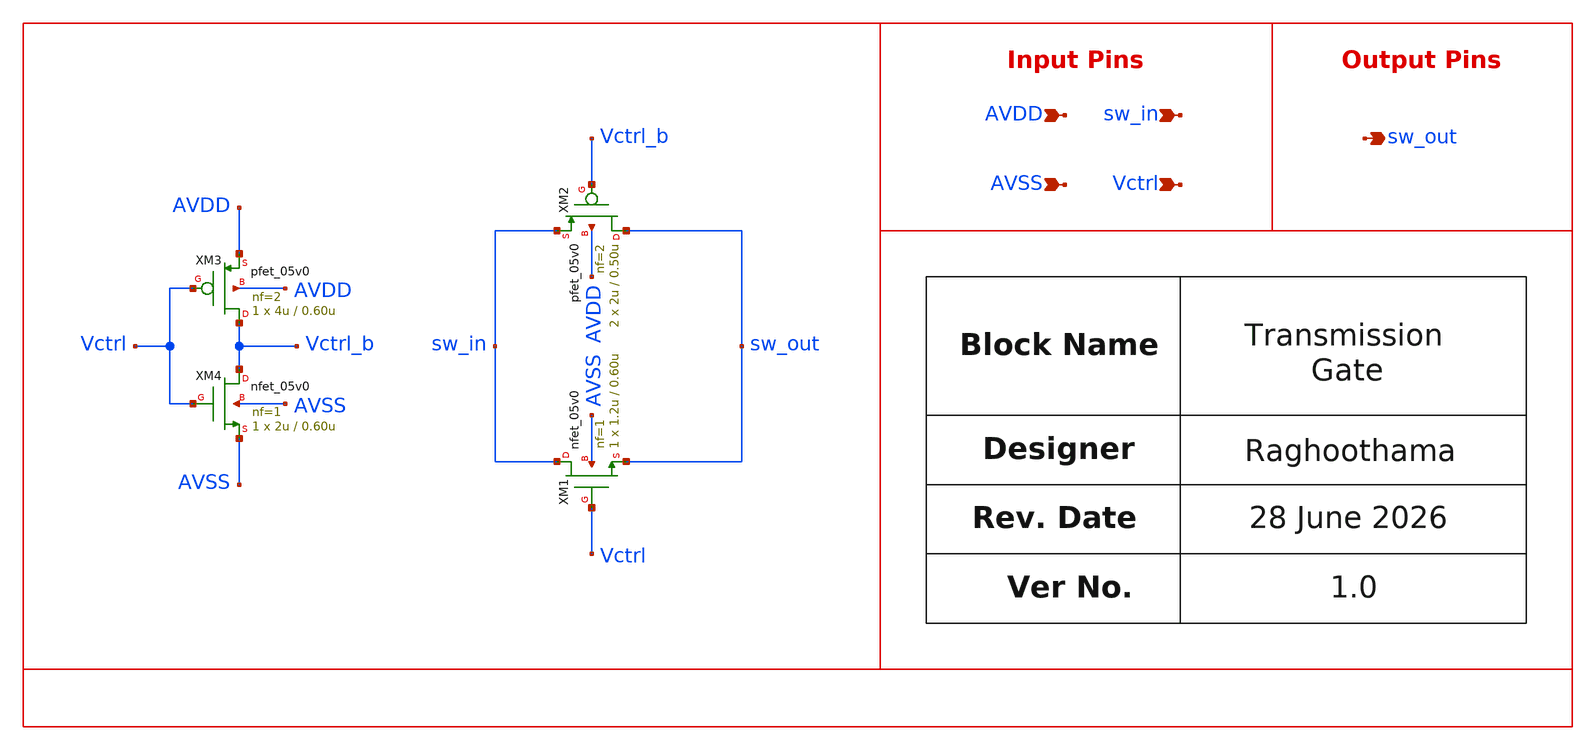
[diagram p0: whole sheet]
** sch_path: design/schematics/ADC/DSM_Loop_filter/second_int/Switches+TG+Cap/rr_cic_bms_afe_iadc_tg_switch.sch
**.subckt rr_cic_bms_afe_iadc_tg_switch sw_in sw_out Vctrl AVDD AVSS
*.ipin sw_in
*.opin sw_out
*.ipin Vctrl
*.ipin AVDD
*.ipin AVSS
XM1 sw_in Vctrl sw_out AVSS nfet_05v0 L=0.60u W=1.2u nf=1 ad='int((nf+1)/2) * W/nf * 0.18u' as='int((nf+2)/2) * W/nf * 0.18u'
+ pd='2*int((nf+1)/2) * (W/nf + 0.18u)' ps='2*int((nf+2)/2) * (W/nf + 0.18u)' nrd='0.18u / W' nrs='0.18u / W'
+ sa=0 sb=0 sd=0 m=1
XM2 sw_out Vctrl_b sw_in AVDD pfet_05v0 L=0.50u W=2u nf=2 ad='int((nf+1)/2) * W/nf * 0.18u' as='int((nf+2)/2) * W/nf * 0.18u'
+ pd='2*int((nf+1)/2) * (W/nf + 0.18u)' ps='2*int((nf+2)/2) * (W/nf + 0.18u)' nrd='0.18u / W' nrs='0.18u / W'
+ sa=0 sb=0 sd=0 m=2
XM3 Vctrl_b Vctrl AVDD AVDD pfet_05v0 L=0.60u W=4u nf=2 ad='int((nf+1)/2) * W/nf * 0.18u' as='int((nf+2)/2) * W/nf * 0.18u'
+ pd='2*int((nf+1)/2) * (W/nf + 0.18u)' ps='2*int((nf+2)/2) * (W/nf + 0.18u)' nrd='0.18u / W' nrs='0.18u / W'
+ sa=0 sb=0 sd=0 m=1
XM4 Vctrl_b Vctrl AVSS AVSS nfet_05v0 L=0.60u W=2u nf=1 ad='int((nf+1)/2) * W/nf * 0.18u' as='int((nf+2)/2) * W/nf * 0.18u'
+ pd='2*int((nf+1)/2) * (W/nf + 0.18u)' ps='2*int((nf+2)/2) * (W/nf + 0.18u)' nrd='0.18u / W' nrs='0.18u / W'
+ sa=0 sb=0 sd=0 m=1
**.ends
.end
